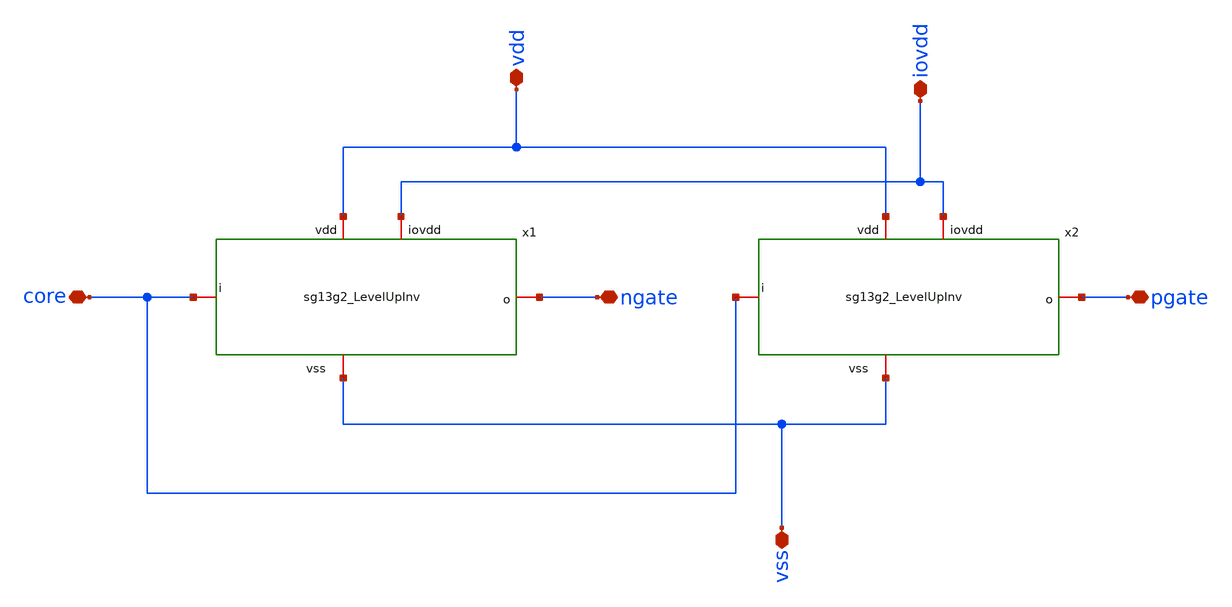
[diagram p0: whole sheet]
** sch_path: ihp-sg13g2/libs.ref/sg13g2_io/xschem/sg13g2_GateLevelUpInv.sch
**.subckt sg13g2_GateLevelUpInv vdd iovdd core vss pgate ngate
*.iopin vdd
*.iopin iovdd
*.iopin core
*.iopin vss
*.iopin pgate
*.iopin ngate
x1 iovdd vdd ngate core vss sg13g2_LevelUpInv
x2 iovdd vdd pgate core vss sg13g2_LevelUpInv
**.ends
.end
